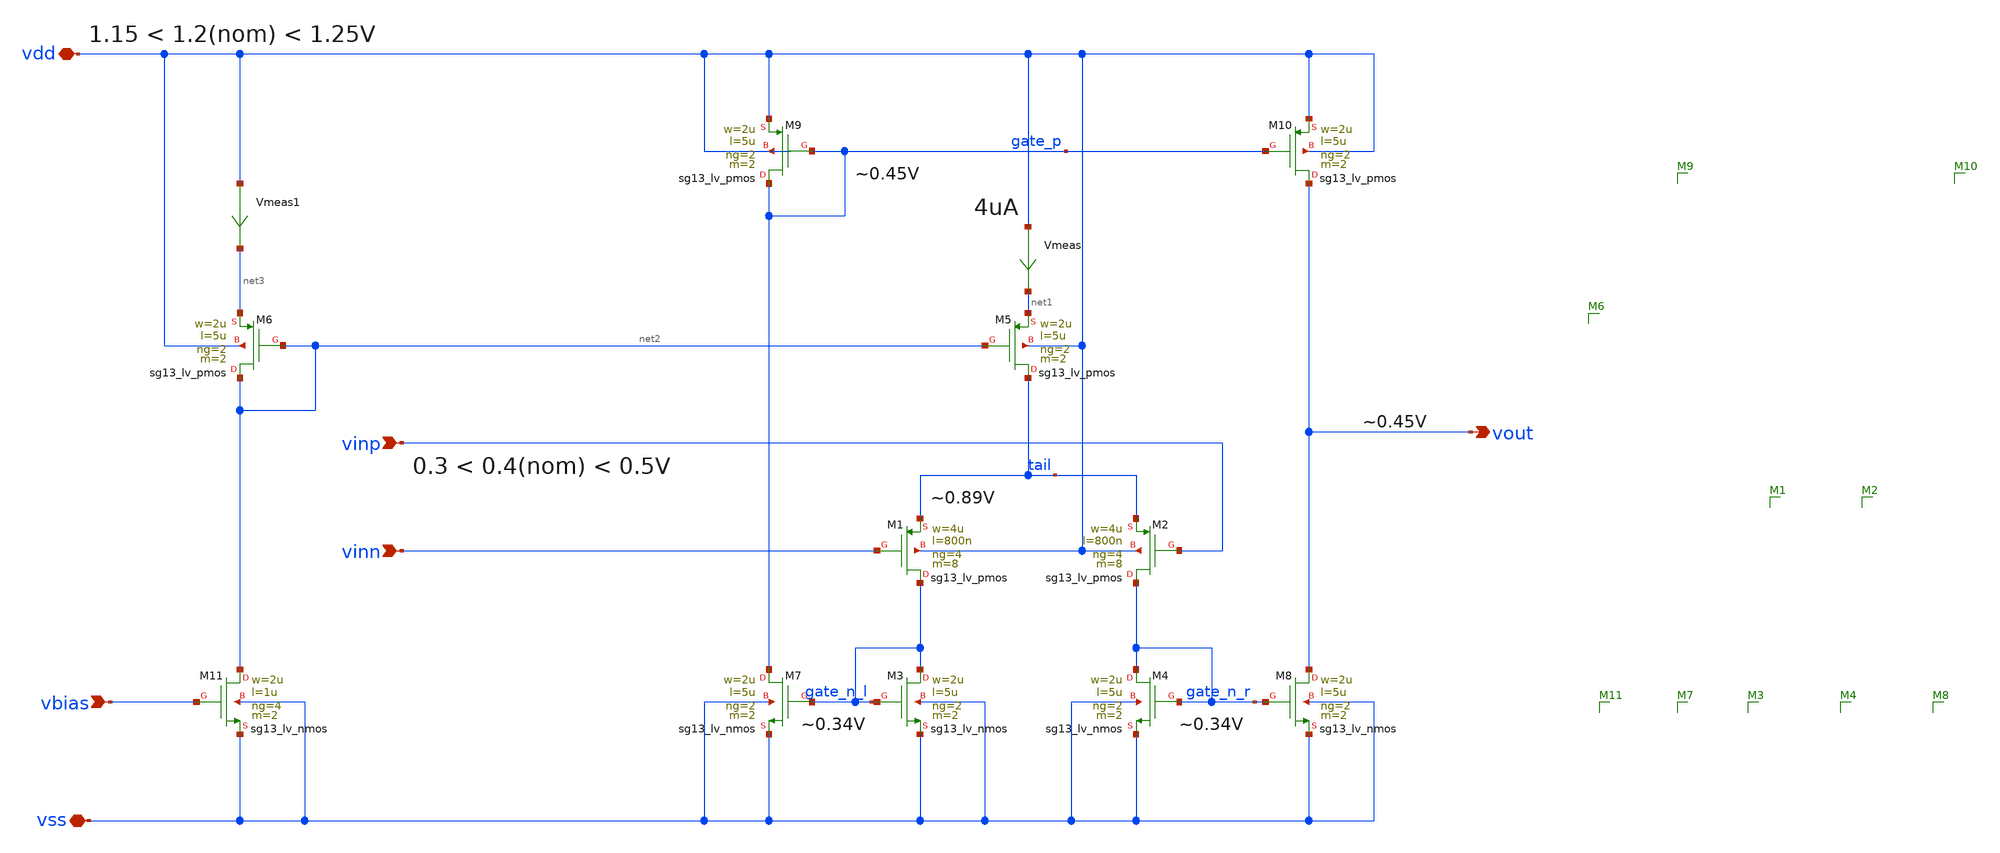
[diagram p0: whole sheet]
** sch_path: v2_feature_extr/ota_p_wr_sim.sch
* (c) 2026 Arianna Rubino, Apache-2.0 license
**.subckt ota_p_wr_sim vinp vinn vbias vdd vss vout
*.ipin vinp
*.ipin vinn
*.ipin vbias
*.iopin vdd
*.iopin vss
*.opin vout
XM3 gate_n_l gate_n_l vss vss sg13_lv_nmos w=2u l=5u ng=2 m=2 mm_ok=1
XM1 gate_n_l vinn tail vdd sg13_lv_pmos w=4u l=800n ng=4 m=8 mm_ok=1
XM2 gate_n_r vinp tail vdd sg13_lv_pmos w=4u l=800n ng=4 m=8 mm_ok=1
XM5 tail net2 net1 vdd sg13_lv_pmos w=2u l=5u ng=2 m=2 mm_ok=1
XM4 gate_n_r gate_n_r vss vss sg13_lv_nmos w=2u l=5u ng=2 m=2 mm_ok=1
XM9 gate_p gate_p vdd vdd sg13_lv_pmos w=2u l=5u ng=2 m=2 mm_ok=1
XM10 vout gate_p vdd vdd sg13_lv_pmos w=2u l=5u ng=2 m=2 mm_ok=1
XM7 gate_p gate_n_l vss vss sg13_lv_nmos w=2u l=5u ng=2 m=2 mm_ok=1
XM8 vout gate_n_r vss vss sg13_lv_nmos w=2u l=5u ng=2 m=2 mm_ok=1
Vmeas vdd net1 0
.save i(vmeas)
XM6 net2 net2 net3 vdd sg13_lv_pmos w=2u l=5u ng=2 m=2 mm_ok=1
XM11 net2 vbias vss vss sg13_lv_nmos w=2u l=1u ng=4 m=2 mm_ok=1
Vmeas1 vdd net3 0
.save i(vmeas1)
**.ends
.end
